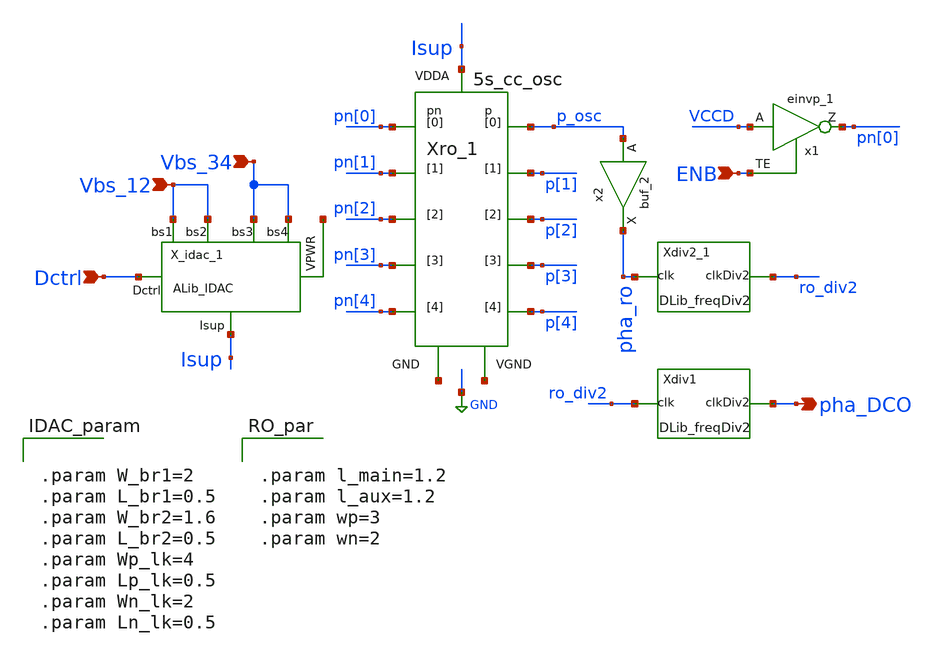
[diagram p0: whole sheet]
** sch_path: xschem/lib/ALib_DCO.sch
**.subckt ALib_DCO Dctrl Vbs_12 Vbs_34 pha_DCO ENB
*.ipin Dctrl
*.ipin Vbs_12
*.ipin Vbs_34
*.opin pha_DCO
*.ipin ENB
x1 VCCD ENB GND GND VCCD VCCD pn[0] sky130_fd_sc_hd__einvp_1
X_idac_1 Dctrl Vbs_12 Vbs_12 Vbs_34 Vbs_34 net1 Isup ALib_IDAC W_br1="W_br1" L_br1="L_br1"
+ W_br2="W_br2" L_br2="L_br2" Wp_lk="Wp_lk" Lp_lk="Lp_lk" Wn_lk="Wn_lk" Ln_lk="Wn_lk"
x2 p_osc GND GND VCCD VCCD pha_ro sky130_fd_sc_hd__buf_2
Xdiv2_1 pha_ro GND GND VCCD VCCD ro_div2 DLib_freqDiv2
Xro_1 net2 Isup p_osc p[1] p[2] p[3] p[4] pn[0] pn[1] pn[2] pn[3] pn[4] net3 5s_cc_osc
Xdiv1 ro_div2 GND GND VCCD VCCD pha_DCO DLib_freqDiv2
**** begin user architecture code


.param W_br1=2
.param L_br1=0.5
.param W_br2=1.6
.param L_br2=0.5
.param Wp_lk=4
.param Lp_lk=0.5
.param Wn_lk=2
.param Ln_lk=0.5

**** end user architecture code
**.ends
.GLOBAL GND
**** begin user architecture code


.param l_main=1.2
.param l_aux=1.2
.param wp=3
.param wn=2

**** end user architecture code
.end
